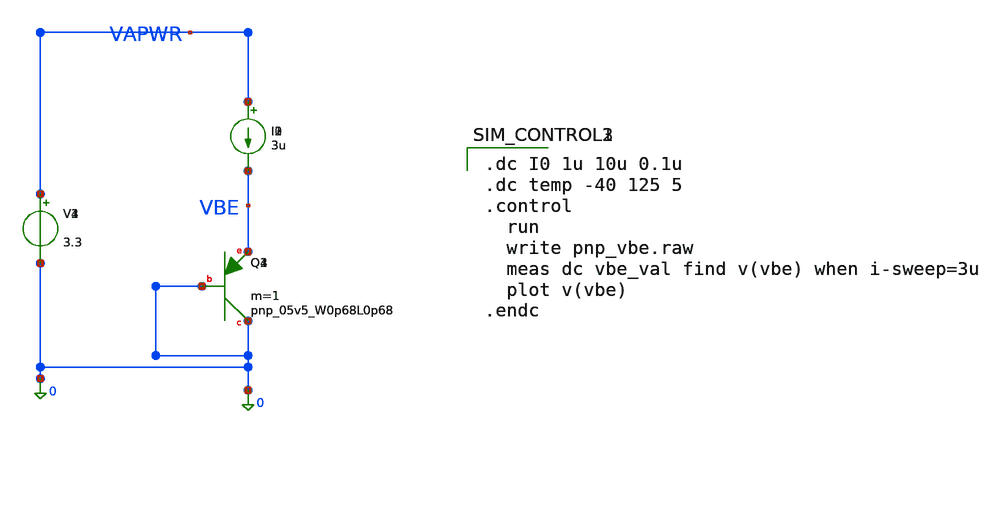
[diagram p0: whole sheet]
** sch_path: designs/bgr_ldo/bgr/pnp_vbe.sch
**.subckt pnp_vbe
XQ1 0 0 VBE sky130_fd_pr__pnp_05v5_W0p68L0p68 m=1
V1 VAPWR 0 3.3
I0 VAPWR VBE 3u
XQ2 0 0 VBE sky130_fd_pr__pnp_05v5_W0p68L0p68 m=1
V2 VAPWR 0 3.3
I1 VAPWR VBE 3u
XQ3 0 0 VBE sky130_fd_pr__pnp_05v5_W0p68L0p68 m=1
V3 VAPWR 0 3.3
I2 VAPWR VBE 3u
XQ4 0 0 VBE sky130_fd_pr__pnp_05v5_W0p68L0p68 m=1
V4 VAPWR 0 3.3
I3 VAPWR VBE 3u
**** begin user architecture code

.dc I0 1u 10u 0.1u
.dc temp -40 125 5
.control
  run
  write pnp_vbe.raw
  meas dc vbe_val find v(vbe) when i-sweep=3u
  plot v(vbe)
.endc


** opencircuitdesign pdks install
.lib $::SKYWATER_MODELS/sky130.lib.spice tt


.dc I0 1u 10u 0.1u
.dc temp -40 125 5
.control
  run
  write pnp_vbe.raw
  meas dc vbe_val find v(vbe) when i-sweep=3u
  plot v(vbe)
.endc


** opencircuitdesign pdks install
.lib $::SKYWATER_MODELS/sky130.lib.spice tt


.dc I0 1u 10u 0.1u
.dc temp -40 125 5
.control
  run
  write pnp_vbe.raw
  meas dc vbe_val find v(vbe) when i-sweep=3u
  plot v(vbe)
.endc


** opencircuitdesign pdks install
.lib $::SKYWATER_MODELS/sky130.lib.spice tt


.dc I0 1u 10u 0.1u
.dc temp -40 125 5
.control
  run
  write pnp_vbe.raw
  meas dc vbe_val find v(vbe) when i-sweep=3u
  plot v(vbe)
.endc


** opencircuitdesign pdks install
.lib $::SKYWATER_MODELS/sky130.lib.spice tt

**** end user architecture code
**.ends
.end
